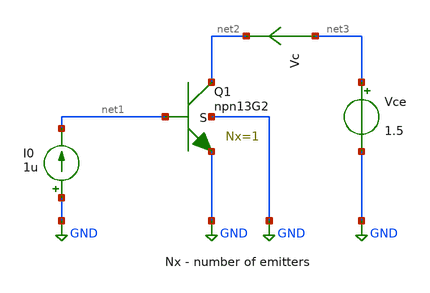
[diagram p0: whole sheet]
** sch_path: ihp-sg13g2/xschem_libs/sg13g2_tests_ase/mc_hbt_13g2/schematic/mc_hbt_13g2.sch
* Copyright 2023 IHP PDK Authors
**.subckt mc_hbt_13g2
Vce net3 GND 1.5
I0 GND net1 1u
Vc net3 net2 0
.save i(vc)
XQ1 net2 net1 GND GND npn13G2 Nx=1 mm_ok=1
**.ends
.GLOBAL GND
.end
